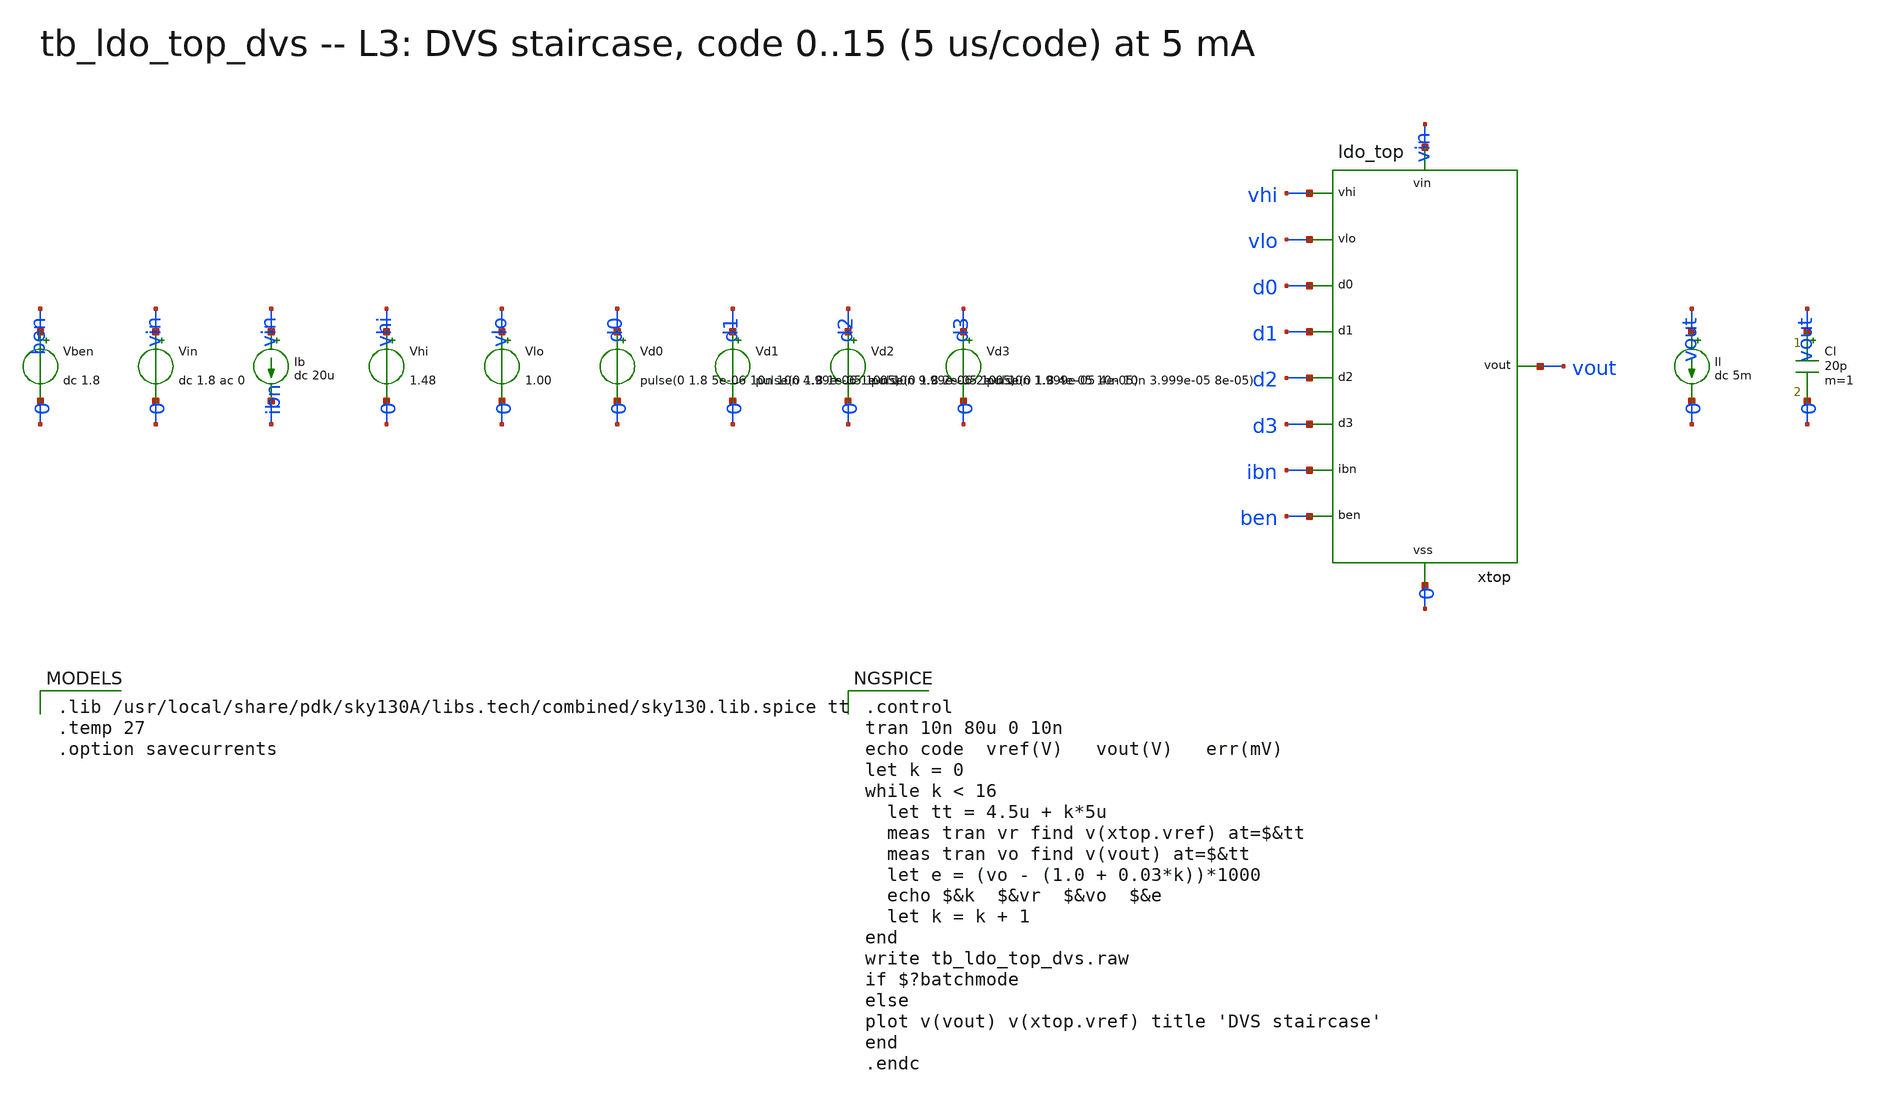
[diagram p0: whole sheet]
** sch_path: xschem/onetops_tb/tb_ldo_top_dvs.sch
**.subckt tb_ldo_top_dvs
Vin vin 0 dc 1.8 ac 0
Ib vin ibn dc 20u
Vben ben 0 dc 1.8
Vhi vhi 0 1.48
Vlo vlo 0 1.00
Vd0 d0 0 pulse(0 1.8 5e-06 10n 10n 4.99e-06 1e-05)
Vd1 d1 0 pulse(0 1.8 1e-05 10n 10n 9.99e-06 2e-05)
Vd2 d2 0 pulse(0 1.8 2e-05 10n 10n 1.999e-05 4e-05)
Vd3 d3 0 pulse(0 1.8 4e-05 10n 10n 3.999e-05 8e-05)
xtop vhi vlo d0 d1 d2 d3 ibn ben vout vin 0 ldo_top
Il vout 0 dc 5m
Cl vout 0 20p m=1
**** begin user architecture code

.lib /usr/local/share/pdk/sky130A/libs.tech/combined/sky130.lib.spice tt
.temp 27
.option savecurrents


.control
tran 10n 80u 0 10n
echo code  vref(V)   vout(V)   err(mV)
let k = 0
while k < 16
  let tt = 4.5u + k*5u
  meas tran vr find v(xtop.vref) at=$&tt
  meas tran vo find v(vout) at=$&tt
  let e = (vo - (1.0 + 0.03*k))*1000
  echo $&k  $&vr  $&vo  $&e
  let k = k + 1
end
write tb_ldo_top_dvs.raw
if $?batchmode
else
plot v(vout) v(xtop.vref) title 'DVS staircase'
end
.endc

**** end user architecture code
**.ends

* expanding   symbol:  onetops/ldo_top.sym # of pins=11
** sym_path: xschem/onetops/ldo_top.sym
** sch_path: xschem/onetops/ldo_top.sch
.subckt ldo_top vhi vlo d0 d1 d2 d3 ibn ben vout vin vss
*.ipin d0
*.ipin d1
*.ipin d2
*.ipin d3
*.ipin ibn
*.ipin ben
*.iopin vhi
*.iopin vlo
*.iopin vout
*.iopin vin
*.iopin vss
xdac vhi vlo d0 d1 d2 d3 vref vin vss rdac4
xcore vref ibn ben vout vin vss ldo_core
.ends


* expanding   symbol:  onetops/rdac4.sym # of pins=9
** sym_path: xschem/onetops/rdac4.sym
** sch_path: xschem/onetops/rdac4.sch
.subckt rdac4 vhi vlo d0 d1 d2 d3 out vdd vss
*.ipin d0
*.ipin d1
*.ipin d2
*.ipin d3
*.opin out
*.iopin vhi
*.iopin vlo
*.iopin vdd
*.iopin vss
R0 t1 vlo 10k m=1
R1 t2 t1 10k m=1
R2 t3 t2 10k m=1
R3 t4 t3 10k m=1
R4 t5 t4 10k m=1
R5 t6 t5 10k m=1
R6 t7 t6 10k m=1
R7 t8 t7 10k m=1
R8 t9 t8 10k m=1
R9 t10 t9 10k m=1
R10 t11 t10 10k m=1
R11 t12 t11 10k m=1
R12 t13 t12 10k m=1
R13 t14 t13 10k m=1
R14 t15 t14 10k m=1
R15 vhi t15 10k m=1
xinv0 d0 d0b vdd vss inv
xinv1 d1 d1b vdd vss inv
xinv2 d2 d2b vdd vss inv
xinv3 d3 d3b vdd vss inv
xm0_0 vlo t1 d0 d0b n1_0 vdd vss mux2_tg
xm0_1 t2 t3 d0 d0b n1_1 vdd vss mux2_tg
xm0_2 t4 t5 d0 d0b n1_2 vdd vss mux2_tg
xm0_3 t6 t7 d0 d0b n1_3 vdd vss mux2_tg
xm0_4 t8 t9 d0 d0b n1_4 vdd vss mux2_tg
xm0_5 t10 t11 d0 d0b n1_5 vdd vss mux2_tg
xm0_6 t12 t13 d0 d0b n1_6 vdd vss mux2_tg
xm0_7 t14 t15 d0 d0b n1_7 vdd vss mux2_tg
xm1_0 n1_0 n1_1 d1 d1b n2_0 vdd vss mux2_tg
xm1_1 n1_2 n1_3 d1 d1b n2_1 vdd vss mux2_tg
xm1_2 n1_4 n1_5 d1 d1b n2_2 vdd vss mux2_tg
xm1_3 n1_6 n1_7 d1 d1b n2_3 vdd vss mux2_tg
xm2_0 n2_0 n2_1 d2 d2b n3_0 vdd vss mux2_tg
xm2_1 n2_2 n2_3 d2 d2b n3_1 vdd vss mux2_tg
xm3_0 n3_0 n3_1 d3 d3b out vdd vss mux2_tg
.ends


* expanding   symbol:  onetops/ldo_core.sym # of pins=6
** sym_path: xschem/onetops/ldo_core.sym
** sch_path: xschem/onetops/ldo_core.sch
.subckt ldo_core vref ibn ben vout vin vss
*.ipin vref
*.ipin ibn
*.ipin ben
*.iopin vout
*.iopin vin
*.iopin vss
xbias ibn x i_pd i_tail i_bu i_dz vss bias_mirror
xboost ibn ben i_bu i_dz x vin vout vss tr_boost
xvset vref i_pd i_tail vset vin vset_gen
xfvf vset x vout fvf_core
xprobe x xg lg_probe
xpass xg vout vin pass_pmos
xcomp x vout comp_rc
.ends


* expanding   symbol:  onetops/inv.sym # of pins=4
** sym_path: xschem/onetops/inv.sym
** sch_path: xschem/onetops/inv.sch
.subckt inv a y vdd vss
*.ipin a
*.opin y
*.iopin vdd
*.iopin vss
XMP1 y a vdd vdd sky130_fd_pr__pfet_01v8 L=0.15 W=2 nf=1 ad='int((1 + 1)/2) * 2 / 1 * 0.29' as='int((1 + 2)/2) * 2 / 1 * 0.29'
+ pd='2*int((1 + 1)/2) * (2 / 1 + 0.29)' ps='2*int((1 + 2)/2) * (2 / 1 + 0.29)' nrd='0.29 / 2 ' nrs='0.29 / 2 '
+ sa=0 sb=0 sd=0 mult=1 m=1
XMN1 y a vss vss sky130_fd_pr__nfet_01v8 L=0.15 W=1 nf=1 ad='int((1 + 1)/2) * 1 / 1 * 0.29' as='int((1 + 2)/2) * 1 / 1 * 0.29'
+ pd='2*int((1 + 1)/2) * (1 / 1 + 0.29)' ps='2*int((1 + 2)/2) * (1 / 1 + 0.29)' nrd='0.29 / 1 ' nrs='0.29 / 1 '
+ sa=0 sb=0 sd=0 mult=1 m=1
.ends


* expanding   symbol:  onetops/mux2_tg.sym # of pins=7
** sym_path: xschem/onetops/mux2_tg.sym
** sch_path: xschem/onetops/mux2_tg.sch
.subckt mux2_tg i0 i1 s sb y vdd vss
*.ipin s
*.ipin sb
*.iopin i0
*.iopin i1
*.iopin y
*.iopin vdd
*.iopin vss
xt0 i0 sb s y vdd vss tgate
xt1 i1 s sb y vdd vss tgate
.ends


* expanding   symbol:  onetops/bias_mirror.sym # of pins=7
** sym_path: xschem/onetops/bias_mirror.sym
** sch_path: xschem/onetops/bias_mirror.sch
.subckt bias_mirror ibn o_fvf o_pd o_tail o_bu o_dz vss
*.ipin ibn
*.opin o_fvf
*.opin o_pd
*.opin o_tail
*.opin o_bu
*.opin o_dz
*.iopin vss
XMN0 ibn ibn vss vss sky130_fd_pr__nfet_01v8 L=1 W=4 nf=1 ad='int((1 + 1)/2) * 4 / 1 * 0.29' as='int((1 + 2)/2) * 4 / 1 * 0.29'
+ pd='2*int((1 + 1)/2) * (4 / 1 + 0.29)' ps='2*int((1 + 2)/2) * (4 / 1 + 0.29)' nrd='0.29 / 4 ' nrs='0.29 / 4 '
+ sa=0 sb=0 sd=0 mult=1 m=1
XMN1 o_fvf ibn vss vss sky130_fd_pr__nfet_01v8 L=1 W=4 nf=1 ad='int((1 + 1)/2) * 4 / 1 * 0.29' as='int((1 + 2)/2) * 4 / 1 * 0.29'
+ pd='2*int((1 + 1)/2) * (4 / 1 + 0.29)' ps='2*int((1 + 2)/2) * (4 / 1 + 0.29)' nrd='0.29 / 4 ' nrs='0.29 / 4 '
+ sa=0 sb=0 sd=0 mult=1 m=1
XMN2 o_bu ibn vss vss sky130_fd_pr__nfet_01v8 L=1 W=4 nf=1 ad='int((1 + 1)/2) * 4 / 1 * 0.29' as='int((1 + 2)/2) * 4 / 1 * 0.29'
+ pd='2*int((1 + 1)/2) * (4 / 1 + 0.29)' ps='2*int((1 + 2)/2) * (4 / 1 + 0.29)' nrd='0.29 / 4 ' nrs='0.29 / 4 '
+ sa=0 sb=0 sd=0 mult=1 m=1
XMN3 o_pd ibn vss vss sky130_fd_pr__nfet_01v8 L=1 W=4 nf=1 ad='int((1 + 1)/2) * 4 / 1 * 0.29' as='int((1 + 2)/2) * 4 / 1 * 0.29'
+ pd='2*int((1 + 1)/2) * (4 / 1 + 0.29)' ps='2*int((1 + 2)/2) * (4 / 1 + 0.29)' nrd='0.29 / 4 ' nrs='0.29 / 4 '
+ sa=0 sb=0 sd=0 mult=1 m=1
XMN4 o_tail ibn vss vss sky130_fd_pr__nfet_01v8 L=1 W=4 nf=1 ad='int((1 + 1)/2) * 4 / 1 * 0.29' as='int((1 + 2)/2) * 4 / 1 * 0.29'
+ pd='2*int((1 + 1)/2) * (4 / 1 + 0.29)' ps='2*int((1 + 2)/2) * (4 / 1 + 0.29)' nrd='0.29 / 4 ' nrs='0.29 / 4 '
+ sa=0 sb=0 sd=0 mult=2 m=2
XMN5 o_dz ibn vss vss sky130_fd_pr__nfet_01v8 L=1 W=4 nf=1 ad='int((1 + 1)/2) * 4 / 1 * 0.29' as='int((1 + 2)/2) * 4 / 1 * 0.29'
+ pd='2*int((1 + 1)/2) * (4 / 1 + 0.29)' ps='2*int((1 + 2)/2) * (4 / 1 + 0.29)' nrd='0.29 / 4 ' nrs='0.29 / 4 '
+ sa=0 sb=0 sd=0 mult=1 m=1
.ends


* expanding   symbol:  onetops/tr_boost.sym # of pins=8
** sym_path: xschem/onetops/tr_boost.sym
** sch_path: xschem/onetops/tr_boost.sch
.subckt tr_boost ibn ben i_bu i_dz x vin vout vss
*.ipin ibn
*.ipin ben
*.iopin i_bu
*.iopin i_dz
*.iopin x
*.iopin vin
*.iopin vout
*.iopin vss
XMPB0 i_bu i_bu vin vin sky130_fd_pr__pfet_01v8_lvt L=0.5 W=40 nf=1 ad='int((1 + 1)/2) * 40 / 1 * 0.29'
+ as='int((1 + 2)/2) * 40 / 1 * 0.29' pd='2*int((1 + 1)/2) * (40 / 1 + 0.29)' ps='2*int((1 + 2)/2) * (40 / 1 + 0.29)'
+ nrd='0.29 / 40 ' nrs='0.29 / 40 ' sa=0 sb=0 sd=0 mult=1 m=1
Rbu i_bu gsu 1Meg m=1
Cbu vout gsu 0.5p m=1
XMPB1 i_dz gsu vin vin sky130_fd_pr__pfet_01v8_lvt L=0.5 W=20 nf=1 ad='int((1 + 1)/2) * 20 / 1 * 0.29'
+ as='int((1 + 2)/2) * 20 / 1 * 0.29' pd='2*int((1 + 1)/2) * (20 / 1 + 0.29)' ps='2*int((1 + 2)/2) * (20 / 1 + 0.29)'
+ nrd='0.29 / 20 ' nrs='0.29 / 20 ' sa=0 sb=0 sd=0 mult=1 m=1
XMNB0 i_dz i_dz vss vss sky130_fd_pr__nfet_01v8 L=0.5 W=2 nf=1 ad='int((1 + 1)/2) * 2 / 1 * 0.29' as='int((1 + 2)/2) * 2 / 1 * 0.29'
+ pd='2*int((1 + 1)/2) * (2 / 1 + 0.29)' ps='2*int((1 + 2)/2) * (2 / 1 + 0.29)' nrd='0.29 / 2 ' nrs='0.29 / 2 '
+ sa=0 sb=0 sd=0 mult=1 m=1
XMNB1 nsw i_dz vss vss sky130_fd_pr__nfet_01v8 L=0.5 W=2 nf=1 ad='int((1 + 1)/2) * 2 / 1 * 0.29' as='int((1 + 2)/2) * 2 / 1 * 0.29'
+ pd='2*int((1 + 1)/2) * (2 / 1 + 0.29)' ps='2*int((1 + 2)/2) * (2 / 1 + 0.29)' nrd='0.29 / 2 ' nrs='0.29 / 2 '
+ sa=0 sb=0 sd=0 mult=20 m=20
XMSW x ben nsw vss sky130_fd_pr__nfet_01v8 L=0.15 W=10 nf=1 ad='int((1 + 1)/2) * 10 / 1 * 0.29' as='int((1 + 2)/2) * 10 / 1 * 0.29'
+ pd='2*int((1 + 1)/2) * (10 / 1 + 0.29)' ps='2*int((1 + 2)/2) * (10 / 1 + 0.29)' nrd='0.29 / 10 ' nrs='0.29 / 10 '
+ sa=0 sb=0 sd=0 mult=1 m=1
Rbo ibn gso 1Meg m=1
Cbo vout gso 0.5p m=1
XMND vout gso vss vss sky130_fd_pr__nfet_01v8 L=1 W=4 nf=1 ad='int((1 + 1)/2) * 4 / 1 * 0.29' as='int((1 + 2)/2) * 4 / 1 * 0.29'
+ pd='2*int((1 + 1)/2) * (4 / 1 + 0.29)' ps='2*int((1 + 2)/2) * (4 / 1 + 0.29)' nrd='0.29 / 4 ' nrs='0.29 / 4 '
+ sa=0 sb=0 sd=0 mult=5 m=5
XMPDZ ndo i_bu vin vin sky130_fd_pr__pfet_01v8_lvt L=0.5 W=40 nf=1 ad='int((1 + 1)/2) * 40 / 1 * 0.29'
+ as='int((1 + 2)/2) * 40 / 1 * 0.29' pd='2*int((1 + 1)/2) * (40 / 1 + 0.29)' ps='2*int((1 + 2)/2) * (40 / 1 + 0.29)'
+ nrd='0.29 / 40 ' nrs='0.29 / 40 ' sa=0 sb=0 sd=0 mult=1 m=1
XMNS1 ndo gso vss vss sky130_fd_pr__nfet_01v8 L=1 W=2 nf=1 ad='int((1 + 1)/2) * 2 / 1 * 0.29' as='int((1 + 2)/2) * 2 / 1 * 0.29'
+ pd='2*int((1 + 1)/2) * (2 / 1 + 0.29)' ps='2*int((1 + 2)/2) * (2 / 1 + 0.29)' nrd='0.29 / 2 ' nrs='0.29 / 2 '
+ sa=0 sb=0 sd=0 mult=1 m=1
XMPO0 ndo ndo vin vin sky130_fd_pr__pfet_01v8 L=0.5 W=4 nf=1 ad='int((1 + 1)/2) * 4 / 1 * 0.29' as='int((1 + 2)/2) * 4 / 1 * 0.29'
+ pd='2*int((1 + 1)/2) * (4 / 1 + 0.29)' ps='2*int((1 + 2)/2) * (4 / 1 + 0.29)' nrd='0.29 / 4 ' nrs='0.29 / 4 '
+ sa=0 sb=0 sd=0 mult=1 m=1
XMPO1 psw ndo vin vin sky130_fd_pr__pfet_01v8 L=0.5 W=4 nf=1 ad='int((1 + 1)/2) * 4 / 1 * 0.29' as='int((1 + 2)/2) * 4 / 1 * 0.29'
+ pd='2*int((1 + 1)/2) * (4 / 1 + 0.29)' ps='2*int((1 + 2)/2) * (4 / 1 + 0.29)' nrd='0.29 / 4 ' nrs='0.29 / 4 '
+ sa=0 sb=0 sd=0 mult=20 m=20
XMPSW x benb psw vin sky130_fd_pr__pfet_01v8 L=0.15 W=20 nf=1 ad='int((1 + 1)/2) * 20 / 1 * 0.29' as='int((1 + 2)/2) * 20 / 1 * 0.29'
+ pd='2*int((1 + 1)/2) * (20 / 1 + 0.29)' ps='2*int((1 + 2)/2) * (20 / 1 + 0.29)' nrd='0.29 / 20 ' nrs='0.29 / 20 '
+ sa=0 sb=0 sd=0 mult=1 m=1
xinv ben benb vin vss inv
.ends


* expanding   symbol:  onetops/vset_gen.sym # of pins=5
** sym_path: xschem/onetops/vset_gen.sym
** sch_path: xschem/onetops/vset_gen.sch
.subckt vset_gen vref i_pd i_tail vset vin
*.ipin vref
*.opin vset
*.iopin i_pd
*.iopin i_tail
*.iopin vin
XMPD i_pd i_pd vin vin sky130_fd_pr__pfet_01v8_lvt L=2 W=10 nf=1 ad='int((1 + 1)/2) * 10 / 1 * 0.29'
+ as='int((1 + 2)/2) * 10 / 1 * 0.29' pd='2*int((1 + 1)/2) * (10 / 1 + 0.29)' ps='2*int((1 + 2)/2) * (10 / 1 + 0.29)'
+ nrd='0.29 / 10 ' nrs='0.29 / 10 ' sa=0 sb=0 sd=0 mult=1 m=1
XMPS vrep i_pd vin vin sky130_fd_pr__pfet_01v8_lvt L=2 W=10 nf=1 ad='int((1 + 1)/2) * 10 / 1 * 0.29'
+ as='int((1 + 2)/2) * 10 / 1 * 0.29' pd='2*int((1 + 1)/2) * (10 / 1 + 0.29)' ps='2*int((1 + 2)/2) * (10 / 1 + 0.29)'
+ nrd='0.29 / 10 ' nrs='0.29 / 10 ' sa=0 sb=0 sd=0 mult=1 m=1
XMR 0 vset vrep vrep sky130_fd_pr__pfet_01v8_lvt L=1 W=100 nf=1 ad='int((1 + 1)/2) * 100 / 1 * 0.29'
+ as='int((1 + 2)/2) * 100 / 1 * 0.29' pd='2*int((1 + 1)/2) * (100 / 1 + 0.29)' ps='2*int((1 + 2)/2) * (100 / 1 + 0.29)'
+ nrd='0.29 / 100 ' nrs='0.29 / 100 ' sa=0 sb=0 sd=0 mult=1 m=1
xota vref vrep i_tail vset vin ota5t
Cset vset 0 2p m=1
.ends


* expanding   symbol:  onetops/fvf_core.sym # of pins=3
** sym_path: xschem/onetops/fvf_core.sym
** sch_path: xschem/onetops/fvf_core.sch
.subckt fvf_core vset x vout
*.ipin vset
*.opin x
*.iopin vout
XMC x vset vout vout sky130_fd_pr__pfet_01v8_lvt L=1 W=100 nf=1 ad='int((1 + 1)/2) * 100 / 1 * 0.29'
+ as='int((1 + 2)/2) * 100 / 1 * 0.29' pd='2*int((1 + 1)/2) * (100 / 1 + 0.29)' ps='2*int((1 + 2)/2) * (100 / 1 + 0.29)'
+ nrd='0.29 / 100 ' nrs='0.29 / 100 ' sa=0 sb=0 sd=0 mult=1 m=1
.ends


* expanding   symbol:  onetops/lg_probe.sym # of pins=2
** sym_path: xschem/onetops/lg_probe.sym
** sch_path: xschem/onetops/lg_probe.sch
.subckt lg_probe drv lin
*.iopin drv
*.iopin lin
Vbrk lin drv dc 0 ac 0
Iinj 0 lin dc 0 ac 0
.ends


* expanding   symbol:  onetops/pass_pmos.sym # of pins=3
** sym_path: xschem/onetops/pass_pmos.sym
** sch_path: xschem/onetops/pass_pmos.sch
.subckt pass_pmos g vout vin
*.ipin g
*.iopin vin
*.iopin vout
XMP vout g vin vin sky130_fd_pr__pfet_01v8 L=0.35 W=10 nf=1 ad='int((1 + 1)/2) * 10 / 1 * 0.29' as='int((1 + 2)/2) * 10 / 1 * 0.29'
+ pd='2*int((1 + 1)/2) * (10 / 1 + 0.29)' ps='2*int((1 + 2)/2) * (10 / 1 + 0.29)' nrd='0.29 / 10 ' nrs='0.29 / 10 '
+ sa=0 sb=0 sd=0 mult=70 m=70
.ends


* expanding   symbol:  onetops/comp_rc.sym # of pins=2
** sym_path: xschem/onetops/comp_rc.sym
** sch_path: xschem/onetops/comp_rc.sch
.subckt comp_rc a b
*.iopin a
*.iopin b
Rz a n1 1 m=1
Cc n1 b 4p m=1
.ends


* expanding   symbol:  onetops/tgate.sym # of pins=6
** sym_path: xschem/onetops/tgate.sym
** sch_path: xschem/onetops/tgate.sch
.subckt tgate a en enb b vdd vss
*.ipin en
*.ipin enb
*.iopin a
*.iopin b
*.iopin vdd
*.iopin vss
XMN1 a en b vss sky130_fd_pr__nfet_01v8 L=0.15 W=1 nf=1 ad='int((1 + 1)/2) * 1 / 1 * 0.29' as='int((1 + 2)/2) * 1 / 1 * 0.29'
+ pd='2*int((1 + 1)/2) * (1 / 1 + 0.29)' ps='2*int((1 + 2)/2) * (1 / 1 + 0.29)' nrd='0.29 / 1 ' nrs='0.29 / 1 '
+ sa=0 sb=0 sd=0 mult=1 m=1
XMP1 b enb a vdd sky130_fd_pr__pfet_01v8 L=0.15 W=2 nf=1 ad='int((1 + 1)/2) * 2 / 1 * 0.29' as='int((1 + 2)/2) * 2 / 1 * 0.29'
+ pd='2*int((1 + 1)/2) * (2 / 1 + 0.29)' ps='2*int((1 + 2)/2) * (2 / 1 + 0.29)' nrd='0.29 / 2 ' nrs='0.29 / 2 '
+ sa=0 sb=0 sd=0 mult=1 m=1
.ends


* expanding   symbol:  onetops/ota5t.sym # of pins=5
** sym_path: xschem/onetops/ota5t.sym
** sch_path: xschem/onetops/ota5t.sch
.subckt ota5t inp inn tail out vdd
*.ipin inp
*.ipin inn
*.opin out
*.iopin tail
*.iopin vdd
XMP1 nd nd vdd vdd sky130_fd_pr__pfet_01v8_lvt L=2 W=20 nf=1 ad='int((1 + 1)/2) * 20 / 1 * 0.29' as='int((1 + 2)/2) * 20 / 1 * 0.29'
+ pd='2*int((1 + 1)/2) * (20 / 1 + 0.29)' ps='2*int((1 + 2)/2) * (20 / 1 + 0.29)' nrd='0.29 / 20 ' nrs='0.29 / 20 '
+ sa=0 sb=0 sd=0 mult=1 m=1
XMP2 out nd vdd vdd sky130_fd_pr__pfet_01v8_lvt L=2 W=20 nf=1 ad='int((1 + 1)/2) * 20 / 1 * 0.29' as='int((1 + 2)/2) * 20 / 1 * 0.29'
+ pd='2*int((1 + 1)/2) * (20 / 1 + 0.29)' ps='2*int((1 + 2)/2) * (20 / 1 + 0.29)' nrd='0.29 / 20 ' nrs='0.29 / 20 '
+ sa=0 sb=0 sd=0 mult=1 m=1
XMN1 nd inp tail 0 sky130_fd_pr__nfet_01v8 L=1 W=5 nf=1 ad='int((1 + 1)/2) * 5 / 1 * 0.29' as='int((1 + 2)/2) * 5 / 1 * 0.29'
+ pd='2*int((1 + 1)/2) * (5 / 1 + 0.29)' ps='2*int((1 + 2)/2) * (5 / 1 + 0.29)' nrd='0.29 / 5 ' nrs='0.29 / 5 '
+ sa=0 sb=0 sd=0 mult=1 m=1
XMN2 out inn tail 0 sky130_fd_pr__nfet_01v8 L=1 W=5 nf=1 ad='int((1 + 1)/2) * 5 / 1 * 0.29' as='int((1 + 2)/2) * 5 / 1 * 0.29'
+ pd='2*int((1 + 1)/2) * (5 / 1 + 0.29)' ps='2*int((1 + 2)/2) * (5 / 1 + 0.29)' nrd='0.29 / 5 ' nrs='0.29 / 5 '
+ sa=0 sb=0 sd=0 mult=1 m=1
.ends

.end
